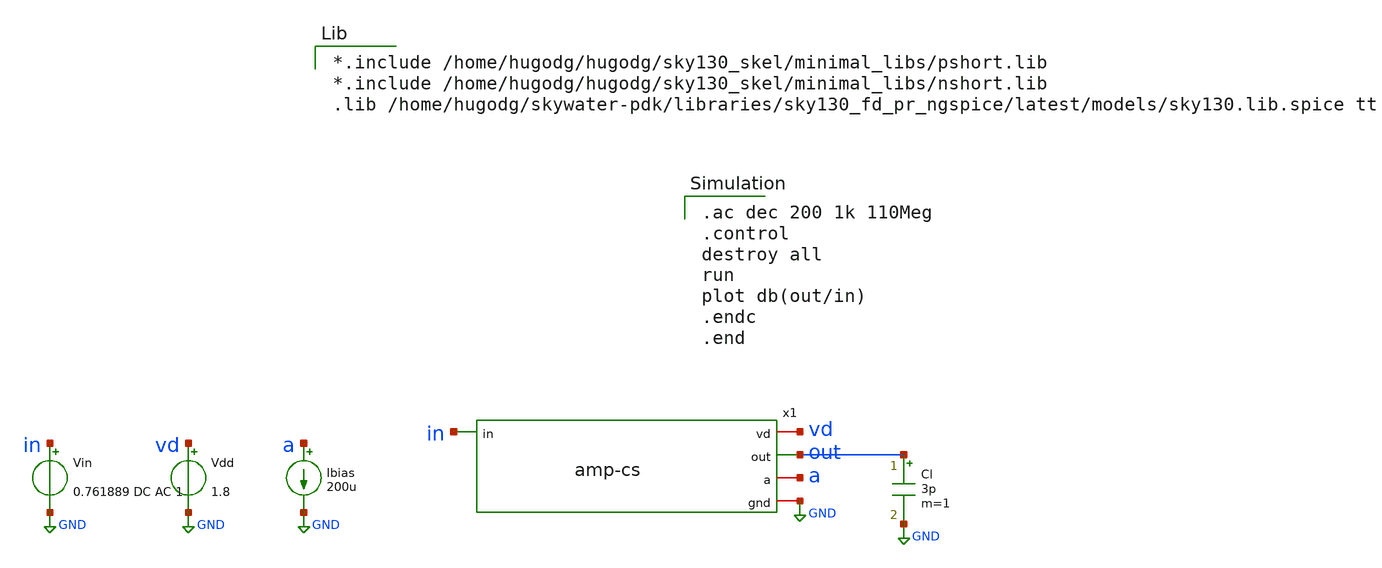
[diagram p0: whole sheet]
** sch_path: xschem/tb-ac.sch
**.subckt tb-ac
x1 vd out a in GND amp-cs
Vin in GND 0.761889 DC AC 1
Vdd vd GND 1.8
Ibias a GND 200u
Cl out GND 3p m=1
**** begin user architecture code

.ac dec 200 1k 110Meg
.control
destroy all
run
plot db(out/in)
.endc
.end


*.include /home/hugodg/hugodg/sky130_skel/minimal_libs/pshort.lib
*.include /home/hugodg/hugodg/sky130_skel/minimal_libs/nshort.lib
.lib /home/hugodg/skywater-pdk/libraries/sky130_fd_pr_ngspice/latest/models/sky130.lib.spice tt

**** end user architecture code
**.ends

* expanding   symbol:  /home/hugodg/projects_sky130/microelectronic/amp-cs/xschem/amp-cs.sym # of
*+ pins=5
** sym_path: xschem/amp-cs.sym
** sch_path: xschem/amp-cs.sch
.subckt amp-cs vd out a in gnd
*.ipin in
*.iopin vd
*.iopin gnd
*.iopin a
*.opin out
XM4 out in gnd gnd sky130_fd_pr__nfet_01v8 L=1 W=43 nf=5 ad='int((nf+1)/2) * W/nf * 0.29' as='int((nf+2)/2) * W/nf * 0.29'
+ pd='2*int((nf+1)/2) * (W/nf + 0.29)' ps='2*int((nf+2)/2) * (W/nf + 0.29)' nrd='0.29 / W' nrs='0.29 / W'
+ sa=0 sb=0 sd=0 mult=1 m=1
XM5 out a vd vd sky130_fd_pr__pfet_01v8 L=1 W=479 nf=10 ad='int((nf+1)/2) * W/nf * 0.29' as='int((nf+2)/2) * W/nf * 0.29'
+ pd='2*int((nf+1)/2) * (W/nf + 0.29)' ps='2*int((nf+2)/2) * (W/nf + 0.29)' nrd='0.29 / W' nrs='0.29 / W'
+ sa=0 sb=0 sd=0 mult=1 m=1
XM2 a a vd vd sky130_fd_pr__pfet_01v8 L=1 W=479 nf=10 ad='int((nf+1)/2) * W/nf * 0.29' as='int((nf+2)/2) * W/nf * 0.29'
+ pd='2*int((nf+1)/2) * (W/nf + 0.29)' ps='2*int((nf+2)/2) * (W/nf + 0.29)' nrd='0.29 / W' nrs='0.29 / W'
+ sa=0 sb=0 sd=0 mult=1 m=1
**** begin user architecture code

C0 A IN 1.92fF
C1 IN vd 11.75fF
C2 A vd 133.60fF

**** end user architecture code
.ends

.GLOBAL GND
.end
